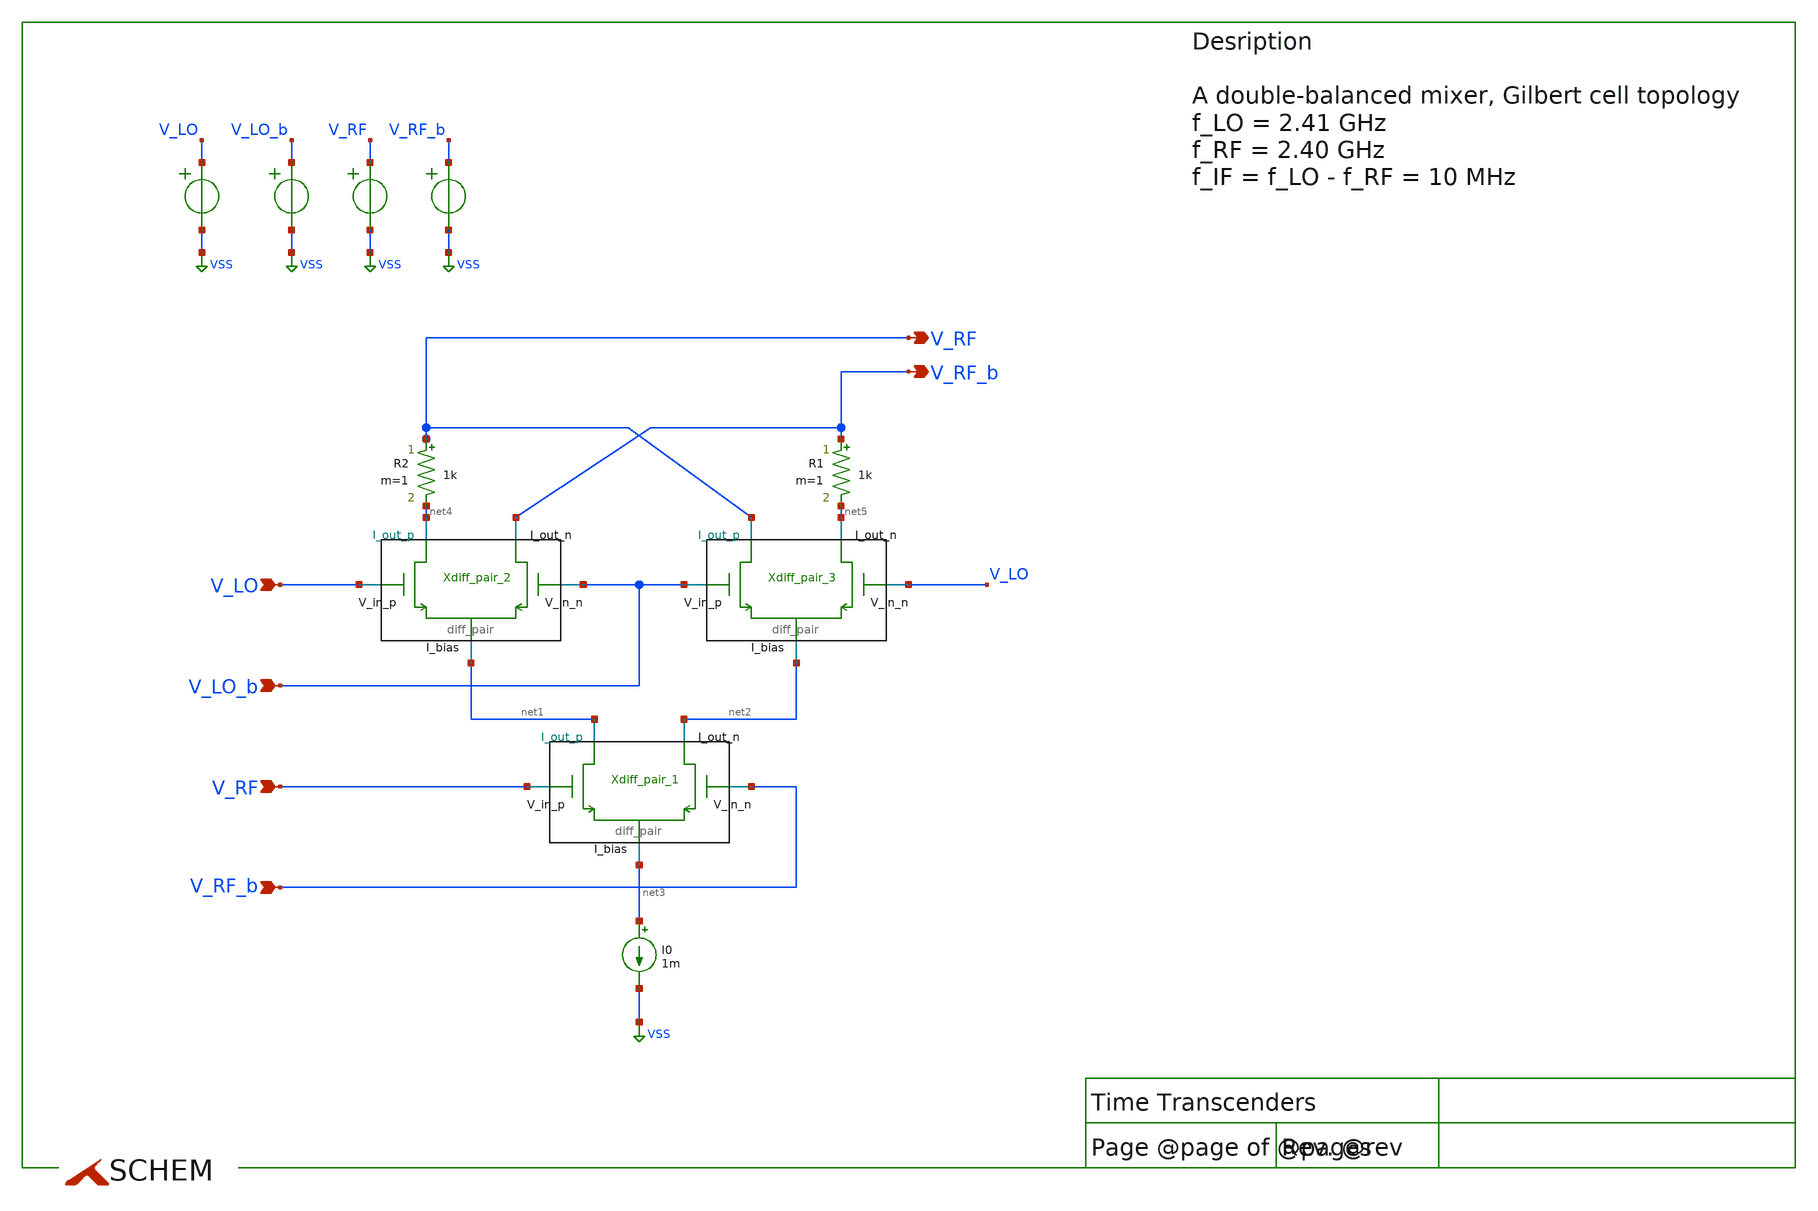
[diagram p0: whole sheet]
** sch_path: src/design_xsch/Gilbert_cell.sch
**.subckt Gilbert_cell V_LO V_LO_b V_RF V_RF_b V_RF V_RF_b
*.ipin V_LO
*.ipin V_LO_b
*.ipin V_RF
*.ipin V_RF_b
*.opin V_RF
*.opin V_RF_b
I0 net3 VSS 1m
E1 V_LO VSS VOL=' '1.5 + sin(time * 2.41 * 1e9)' '
E2 V_LO_b VSS VOL=' '1.5 - sin(time * 2.41 * 1e9)' '
E4 V_RF VSS VOL=' '1.5 + sin(time * 2.40 * 1e9)' '
E6 V_RF_b VSS VOL=' '1.5 - sin(time * 2.40 * 1e9)' '
Xdiff_pair_1 net2 net1 V_RF V_RF_b net3 VSS diff_pair W_neg=0.22u L_neg=0.28u W_pos=0.22u
+ L_pos=0.28u m=1
Xdiff_pair_2 V_RF_b net4 V_LO V_LO_b net1 VSS diff_pair W_neg=0.22u L_neg=0.28u W_pos=0.22u
+ L_pos=0.28u m=1
Xdiff_pair_3 net5 V_RF V_LO_b V_LO net2 VSS diff_pair W_neg=0.22u L_neg=0.28u W_pos=0.22u
+ L_pos=0.28u m=1
R1 V_RF_b net5 1k m=1
R2 V_RF net4 1k m=1
**** begin user architecture code

.include $::180MCU_MODELS/design.ngspice
.lib $::180MCU_MODELS/sm141064.ngspice typical



.temp 27
.control
save all
tran 1p 10n
write Gilbert_sim.raw
.endc


**** end user architecture code
**.ends

* expanding   symbol:  /home/vasil/Downloads/SSCS_PICO_2025/src/design_xsch/diff_pair.sym # of
*+ pins=5
** sym_path: src/design_xsch/diff_pair.sym
** sch_path: src/design_xsch/diff_pair.sch
.subckt diff_pair I_out_n I_out_p V_in_p V_in_n I_bias VSSPIN  mult=1  W_neg=0.22u L_neg=0.28u
+ W_pos=0.22u L_pos=0.28u
*.ipin V_in_p
*.ipin V_in_n
*.iopin I_out_p
*.iopin I_out_n
*.iopin I_bias
XM1 I_out_p V_in_p I_bias VSS nfet_03v3 L=L_pos W=W_pos nf=1 ad='int((nf+1)/2) * W/nf * 0.18u' as='int((nf+2)/2) * W/nf * 0.18u'
+ pd='2*int((nf+1)/2) * (W/nf + 0.18u)' ps='2*int((nf+2)/2) * (W/nf + 0.18u)' nrd='0.18u / W' nrs='0.18u / W'
+ sa=0 sb=0 sd=0 m=mult
XM2 I_out_n V_in_n I_bias VSS nfet_03v3 L=L_neg W=W_neg nf=1 ad='int((nf+1)/2) * W/nf * 0.18u' as='int((nf+2)/2) * W/nf * 0.18u'
+ pd='2*int((nf+1)/2) * (W/nf + 0.18u)' ps='2*int((nf+2)/2) * (W/nf + 0.18u)' nrd='0.18u / W' nrs='0.18u / W'
+ sa=0 sb=0 sd=0 m=mult
.ends

.GLOBAL VSS
.end
